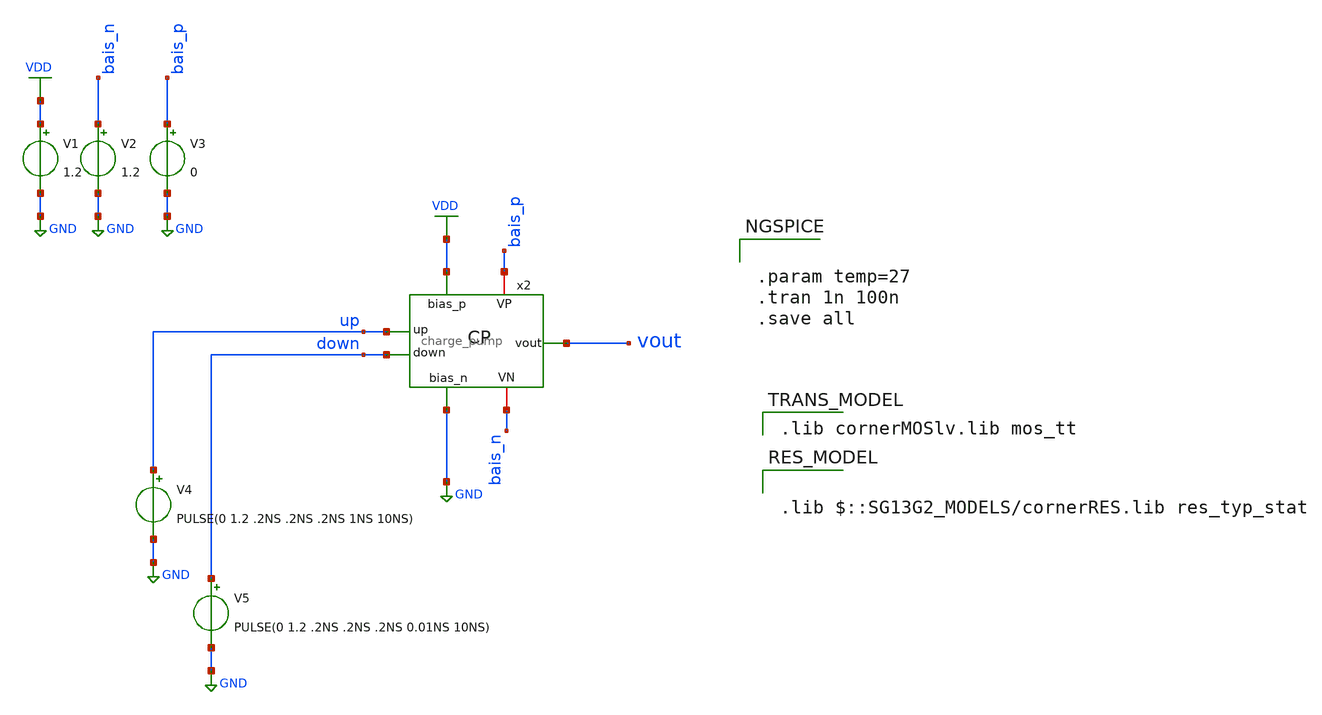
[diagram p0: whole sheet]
** sch_path: Combined Design/design_data/xschem/charge_pump_tb.sch
**.subckt charge_pump_tb
V1 VDD GND 1.2
V2 bais_n GND 1.2
V3 bais_p GND 0
V4 up GND PULSE(0 1.2 .2NS .2NS .2NS 1NS 10NS)
V5 down GND PULSE(0 1.2 .2NS .2NS .2NS 0.01NS 10NS)
x2 bais_p VDD up vout down GND bais_n charge_pump
**** begin user architecture code


.param temp=27
.tran 1n 100n
.save all


 .lib cornerMOSlv.lib mos_tt


.lib $::SG13G2_MODELS/cornerRES.lib res_typ_stat

**** end user architecture code
**.ends

* expanding   symbol:  charge_pump.sym # of pins=7
** sym_path: Combined Design/design_data/xschem/charge_pump.sym
** sch_path: Combined Design/design_data/xschem/charge_pump.sch
.subckt charge_pump VP bias_p up vout down bias_n VN
*.ipin bias_p
*.ipin up
*.ipin down
*.ipin bias_n
*.iopin VN
*.iopin VP
*.opin vout
XM1 net1 bias_n VN VN sg13_lv_nmos w=0.15u l=0.13u ng=1 m=1 mm_ok=1
XM2 vout down net1 VN sg13_lv_nmos w=0.15u l=0.13u ng=1 m=1 mm_ok=1
XM3 vout up net2 VP sg13_lv_pmos w=0.30u l=0.13u ng=1 m=1 mm_ok=1
XM4 net2 bias_p VP VP sg13_lv_pmos w=0.30u l=0.13u ng=1 m=1 mm_ok=1
.ends

.GLOBAL GND
.GLOBAL VDD
.end
